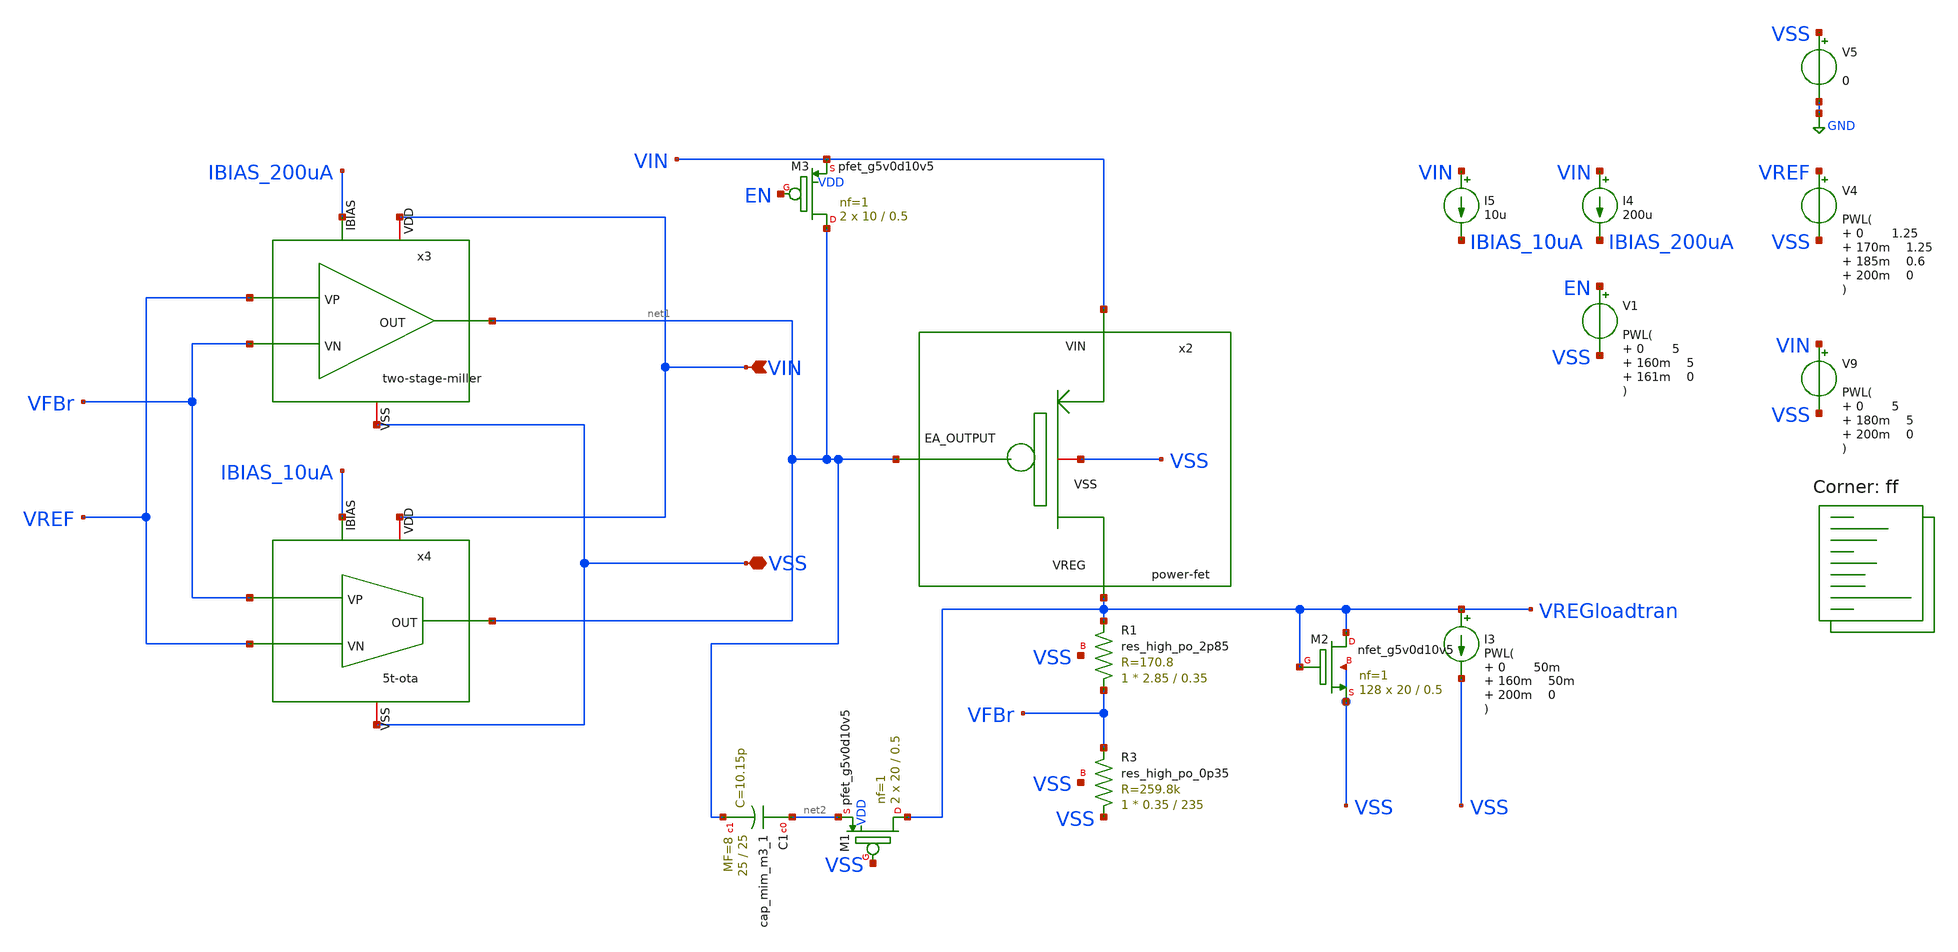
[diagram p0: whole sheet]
** sch_path: bandgap/testbench/tb_tran_turn-off.sch
**.subckt tb_tran_turn-off VIN VSS
*.ipin VIN
*.iopin VSS
x2 VIN VSS net1 VREGloadtran power-fet
XR3 VSS VFBr VSS sky130_fd_pr__res_high_po_0p35 L=235 mult=1 m=1
XR1 VFBr VREGloadtran VSS sky130_fd_pr__res_high_po_2p85 L=0.35 mult=1 m=1
x3 VIN net1 VREF VFBr IBIAS_200uA VSS two-stage-miller
x4 VIN net1 IBIAS_10uA VREF VFBr VSS 5t-ota
I4 VIN IBIAS_200uA 200u
I3 VREGloadtran VSS PWL( 0 50m 160m 50m 200m 0
)
V4 VREF VSS PWL( 0 1.25 170m 1.25 185m 0.6 200m 0
)
V5 VSS GND 0
V9 VIN VSS PWL( 0 5 180m 5 200m 0
)
I5 VIN IBIAS_10uA 10u
XM2 VREGloadtran VREGloadtran VSS VSS sky130_fd_pr__nfet_g5v0d10v5 L=0.5 W=20 nf=1 ad='int((nf+1)/2) * W/nf * 0.29'
+ as='int((nf+2)/2) * W/nf * 0.29' pd='2*int((nf+1)/2) * (W/nf + 0.29)' ps='2*int((nf+2)/2) * (W/nf + 0.29)'
+ nrd='0.29 / W' nrs='0.29 / W' sa=0 sb=0 sd=0 mult=128 m=128
XC1 net2 net1 sky130_fd_pr__cap_mim_m3_1 W=25 L=25 MF=8 m=8
XM1 VREGloadtran VSS net2 VDD sky130_fd_pr__pfet_g5v0d10v5 L=0.5 W=20 nf=1 ad='int((nf+1)/2) * W/nf * 0.29'
+ as='int((nf+2)/2) * W/nf * 0.29' pd='2*int((nf+1)/2) * (W/nf + 0.29)' ps='2*int((nf+2)/2) * (W/nf + 0.29)'
+ nrd='0.29 / W' nrs='0.29 / W' sa=0 sb=0 sd=0 mult=2 m=2
XM3 net1 EN VIN VDD sky130_fd_pr__pfet_g5v0d10v5 L=0.5 W=10 nf=1 ad='int((nf+1)/2) * W/nf * 0.29' as='int((nf+2)/2) * W/nf * 0.29'
+ pd='2*int((nf+1)/2) * (W/nf + 0.29)' ps='2*int((nf+2)/2) * (W/nf + 0.29)' nrd='0.29 / W' nrs='0.29 / W'
+ sa=0 sb=0 sd=0 mult=2 m=2
V1 EN VSS PWL( 0 5 160m 5 161m 0
)
**** begin user architecture code



.temp 27
.control

tran 10u 200m

* Nominal output voltage (from regulation region)
let Vout_nom = 1.25
let Vout_95  = 0.95*Vout_nom

* Find Vin where Vout crosses 95%
meas dc Vin_do find v(vin) when v(vreg)=Vout_95

* Measure Vout at that Vin (for completeness)
meas dc Vout_do find v(vreg) when v(vreg)=Vout_95

* Compute dropout voltage
let Vdo = Vin_do - Vout_do

* Compute overshoot, undershoot and peak-to-peak voltage
meas tran Vout_max MAX v(VREGloadtran)
meas tran Vout_min MIN v(VREGloadtran)
let vpp = Vout_max - Vout_min

print Vin_do Vout_do Vdo
print Vout_max Vout_min Vpp
plot VREGloadtran EN VIN VREF
plot VREGloadtran2
plot VREG
plot VIN
plot I(load)

.endc


.lib $::SKYWATER_MODELS/sky130.lib.spice ff
**** end user architecture code
**.ends
.GLOBAL GND
.end
